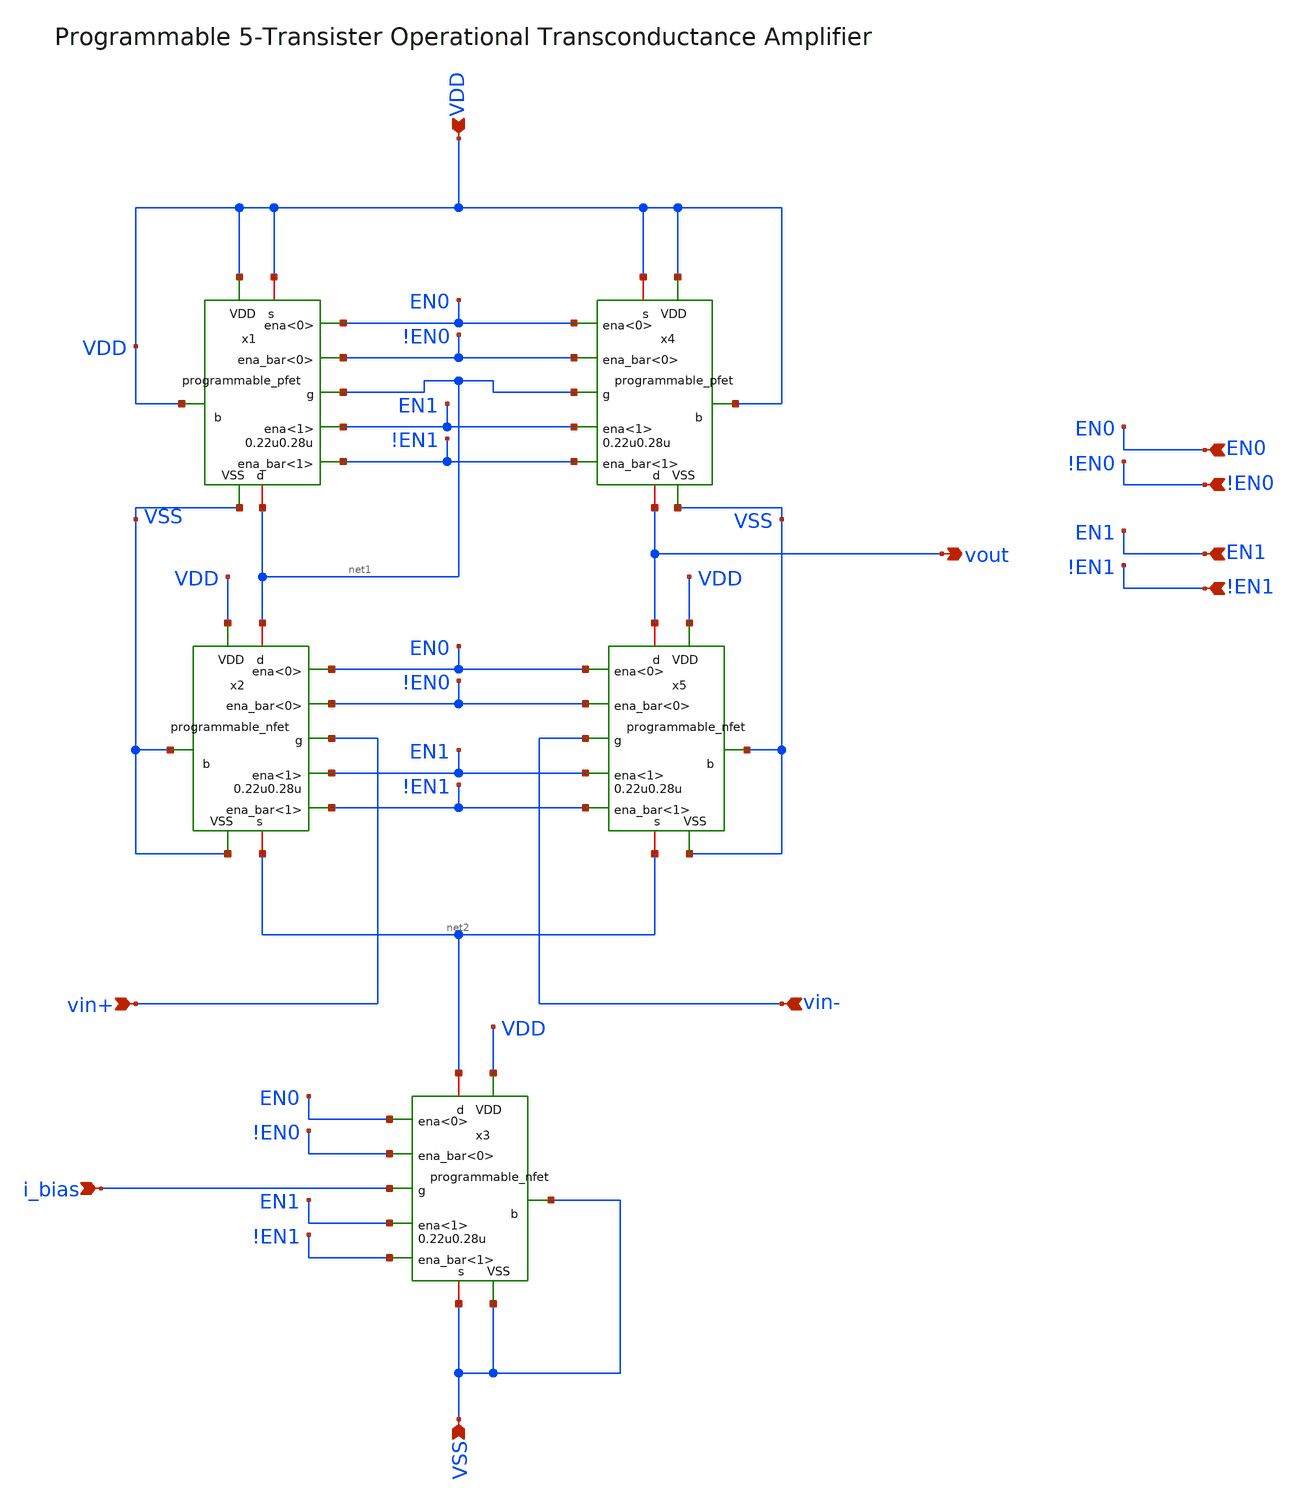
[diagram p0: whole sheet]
** sch_path: designs/libs/core_amps/ota_5t/programmable_5tOTA.sch
**.subckt programmable_5tOTA VDD vout vin+ vin- i_bias VSS EN0 !EN0 EN1 !EN1
*.ipin VDD
*.opin vout
*.ipin vin+
*.ipin vin-
*.ipin i_bias
*.ipin VSS
*.ipin EN0
*.ipin !EN0
*.ipin EN1
*.ipin !EN1
x1 net1 VDD net1 VDD !EN0 VDD !EN1 EN0 EN1 VSS programmable_pfet width=0.22u length=0.28u
x2 net1 VSS vin+ net2 !EN0 VDD !EN1 EN0 EN1 VSS programmable_nfet width=0.22u length=0.28u
x3 net2 VSS i_bias VSS !EN0 VDD !EN1 EN0 EN1 VSS programmable_nfet width=0.22u length=0.28u
x4 vout VDD net1 VDD !EN0 VDD !EN1 EN0 EN1 VSS programmable_pfet width=0.22u length=0.28u
x5 vout VSS vin- net2 !EN0 VDD !EN1 EN0 EN1 VSS programmable_nfet width=0.22u length=0.28u
**.ends
.end
